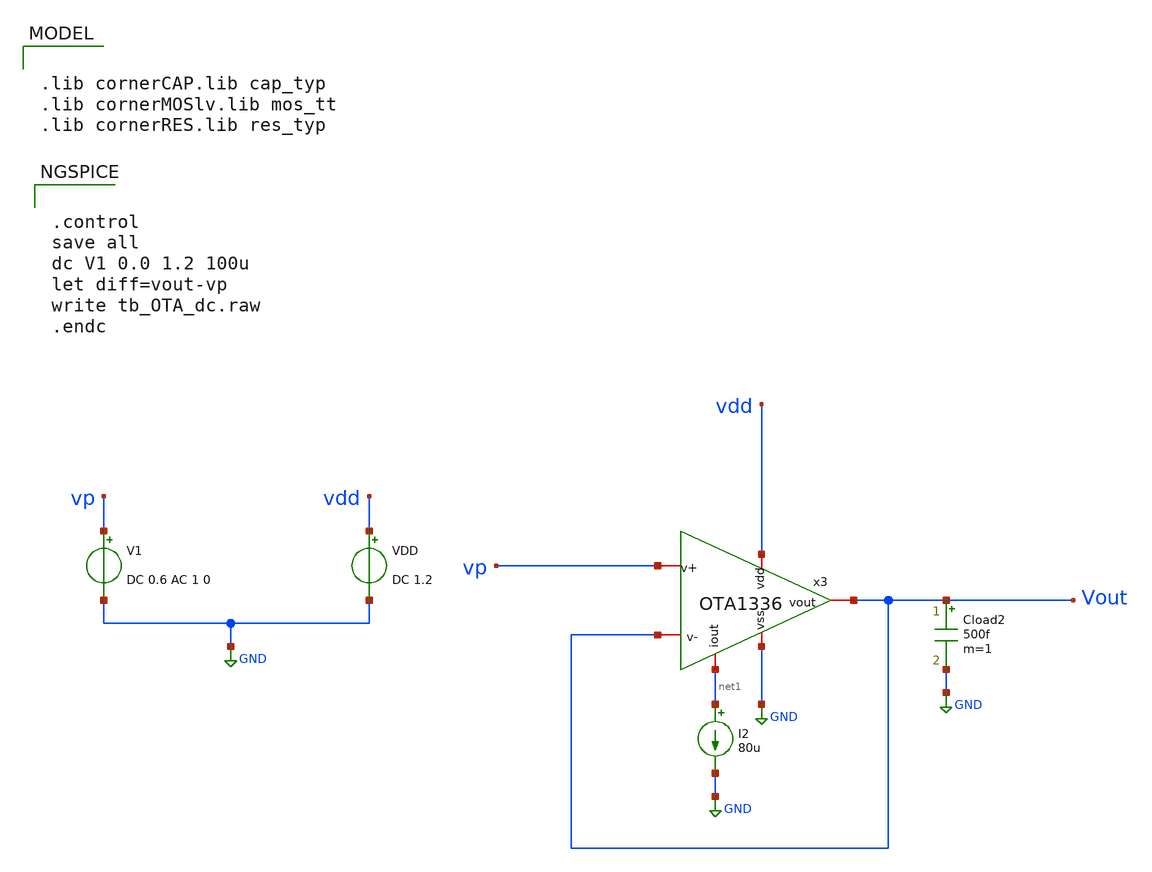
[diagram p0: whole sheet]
** sch_path: OTA1336-main/testbenches/dc/xschem/OTA1336_swing_tb.sch
**.subckt OTA1336_swing_tb
V1 vp GND DC 0.6 AC 1 0
VDD vdd GND DC 1.2
I2 net1 GND 80u
x3 vdd net1 Vout Vout vp GND OTA1336
Cload2 Vout GND 500f m=1
**** begin user architecture code

.lib cornerCAP.lib cap_typ
.lib cornerMOSlv.lib mos_tt
.lib cornerRES.lib res_typ



.control
save all
dc V1 0.0 1.2 100u
let diff=vout-vp
write tb_OTA_dc.raw
.endc


**** end user architecture code
**.ends
.GLOBAL GND
.end
